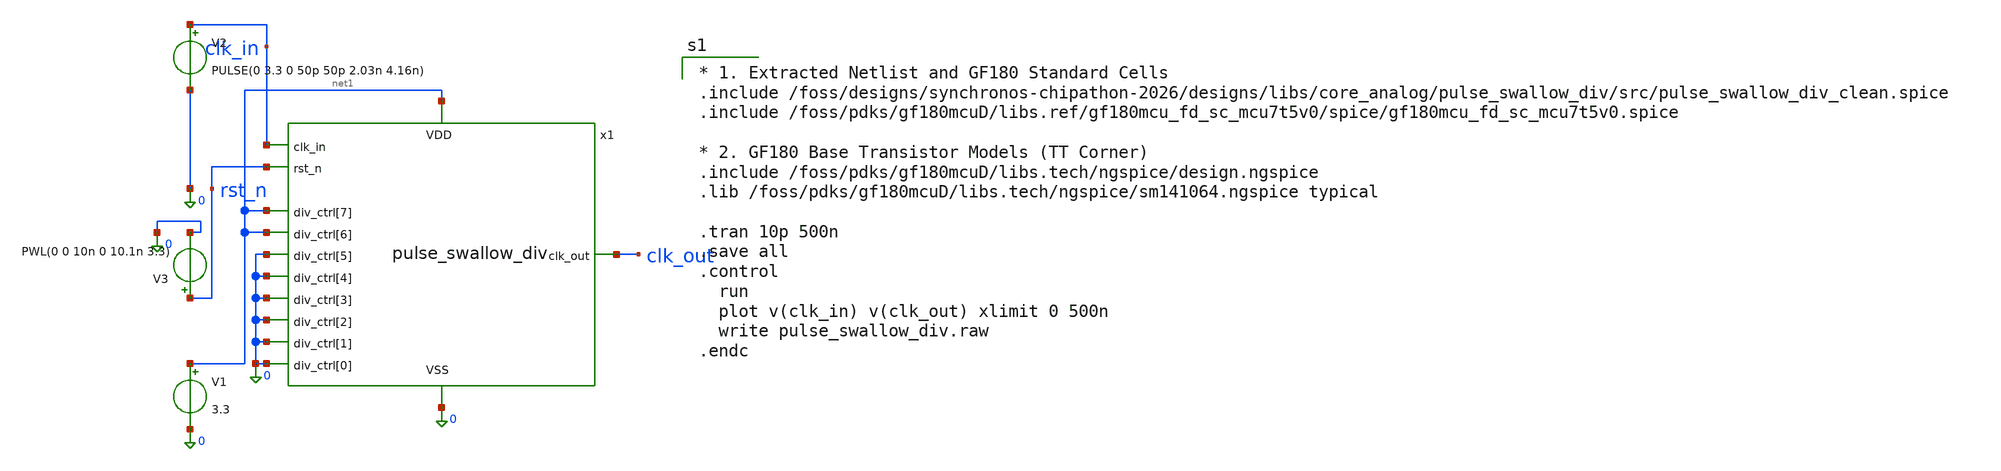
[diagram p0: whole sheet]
** sch_path: designs/libs/tb_analog/tb_pulse_swallow_div/pulse_swallow_tb.sch
**.subckt pulse_swallow_tb
V1 net1 0 3.3
V2 clk_in 0 PULSE(0 3.3 0 50p 50p 2.03n 4.16n)
V3 rst_n 0 PWL(0 0 10n 0 10.1n 3.3)
x1 net1 0 clk_in clk_out 0 0 0 0 0 0 net1 net1 rst_n pulse_swallow_div
**** begin user architecture code

* 1. Extracted Netlist and GF180 Standard Cells
.include /foss/designs/synchronos-chipathon-2026/designs/libs/core_analog/pulse_swallow_div/src/pulse_swallow_div_clean.spice
.include /foss/pdks/gf180mcuD/libs.ref/gf180mcu_fd_sc_mcu7t5v0/spice/gf180mcu_fd_sc_mcu7t5v0.spice

* 2. GF180 Base Transistor Models (TT Corner)
.include /foss/pdks/gf180mcuD/libs.tech/ngspice/design.ngspice
.lib /foss/pdks/gf180mcuD/libs.tech/ngspice/sm141064.ngspice typical

.tran 10p 500n
.save all
.control
  run
  plot v(clk_in) v(clk_out) xlimit 0 500n
  write pulse_swallow_div.raw
.endc

**** end user architecture code
**.ends
.end
